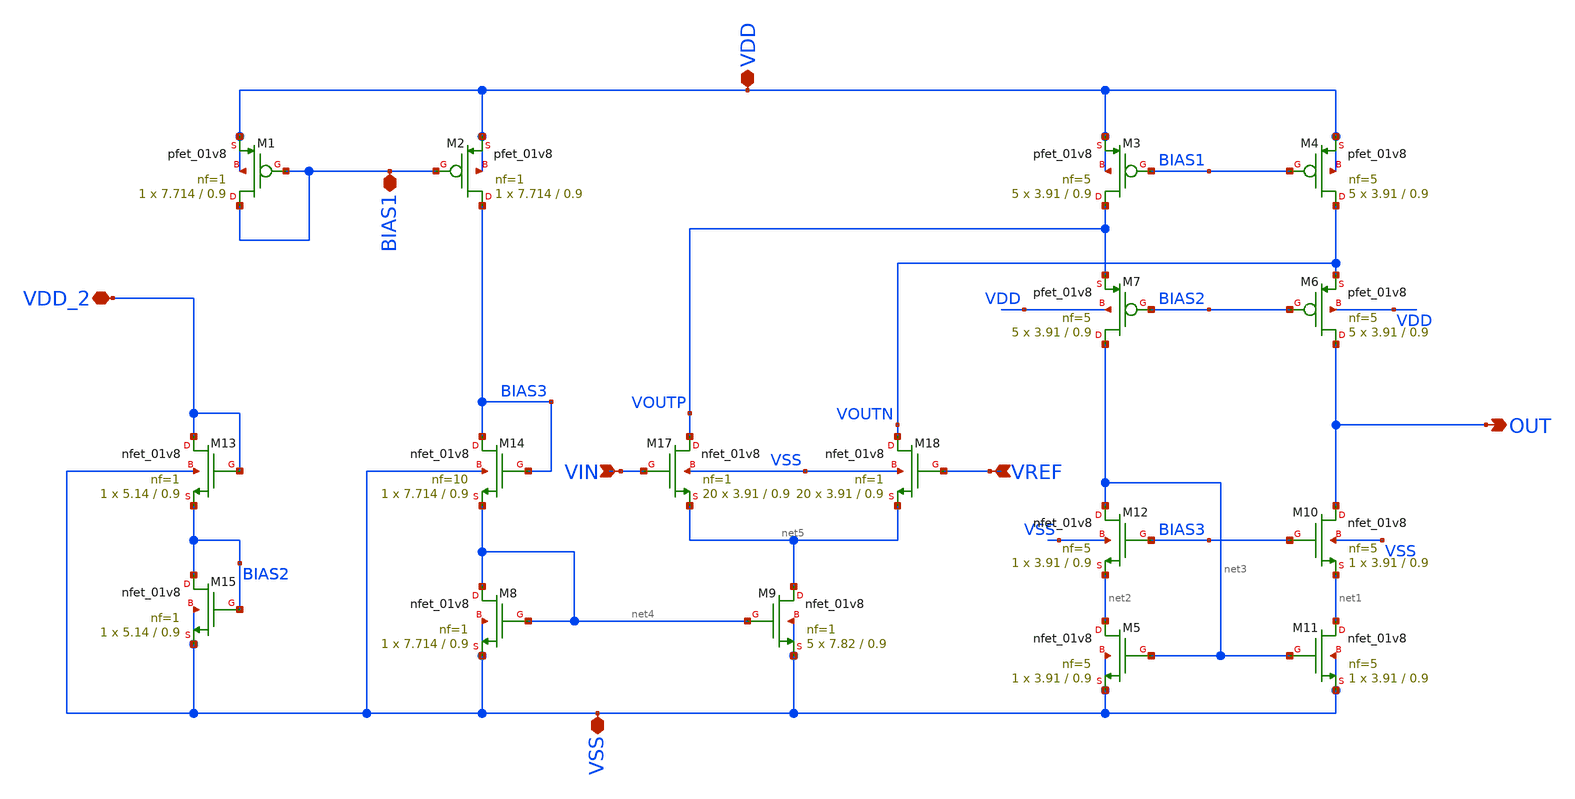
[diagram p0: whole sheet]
** sch_path: xschem/DC_DC_Converter_xschem/OTHERS/DC_DC_Converter_V7/Folded_OPAMP/Folded_OPAMP_previous.sch
**.subckt Folded_OPAMP_previous VSS VDD VDD_2 OUT VIN VREF BIAS1
*.iopin VSS
*.iopin VDD
*.iopin VDD_2
*.opin OUT
*.ipin VIN
*.ipin VREF
*.iopin BIAS1
XM3 VOUTP BIAS1 VDD VDD sky130_fd_pr__pfet_01v8 L=0.9 W=3.91 nf=5 ad='int((nf+1)/2) * W/nf * 0.29' as='int((nf+2)/2) * W/nf * 0.29'
+ pd='2*int((nf+1)/2) * (W/nf + 0.29)' ps='2*int((nf+2)/2) * (W/nf + 0.29)' nrd='0.29 / W' nrs='0.29 / W'
+ sa=0 sb=0 sd=0 mult=5 m=5
XM4 VOUTN BIAS1 VDD VDD sky130_fd_pr__pfet_01v8 L=0.9 W=3.91 nf=5 ad='int((nf+1)/2) * W/nf * 0.29' as='int((nf+2)/2) * W/nf * 0.29'
+ pd='2*int((nf+1)/2) * (W/nf + 0.29)' ps='2*int((nf+2)/2) * (W/nf + 0.29)' nrd='0.29 / W' nrs='0.29 / W'
+ sa=0 sb=0 sd=0 mult=5 m=5
XM6 OUT BIAS2 VOUTN VDD sky130_fd_pr__pfet_01v8 L=0.9 W=3.91 nf=5 ad='int((nf+1)/2) * W/nf * 0.29' as='int((nf+2)/2) * W/nf * 0.29'
+ pd='2*int((nf+1)/2) * (W/nf + 0.29)' ps='2*int((nf+2)/2) * (W/nf + 0.29)' nrd='0.29 / W' nrs='0.29 / W'
+ sa=0 sb=0 sd=0 mult=5 m=5
XM7 net3 BIAS2 VOUTP VDD sky130_fd_pr__pfet_01v8 L=0.9 W=3.91 nf=5 ad='int((nf+1)/2) * W/nf * 0.29' as='int((nf+2)/2) * W/nf * 0.29'
+ pd='2*int((nf+1)/2) * (W/nf + 0.29)' ps='2*int((nf+2)/2) * (W/nf + 0.29)' nrd='0.29 / W' nrs='0.29 / W'
+ sa=0 sb=0 sd=0 mult=5 m=5
XM13 VDD_2 VDD_2 BIAS2 VSS sky130_fd_pr__nfet_01v8 L=0.9 W=5.14 nf=1 ad='int((nf+1)/2) * W/nf * 0.29'
+ as='int((nf+2)/2) * W/nf * 0.29' pd='2*int((nf+1)/2) * (W/nf + 0.29)' ps='2*int((nf+2)/2) * (W/nf + 0.29)'
+ nrd='0.29 / W' nrs='0.29 / W' sa=0 sb=0 sd=0 mult=1 m=1
XM14 BIAS3 BIAS3 net4 VSS sky130_fd_pr__nfet_01v8 L=0.9 W=7.714 nf=10 ad='int((nf+1)/2) * W/nf * 0.29'
+ as='int((nf+2)/2) * W/nf * 0.29' pd='2*int((nf+1)/2) * (W/nf + 0.29)' ps='2*int((nf+2)/2) * (W/nf + 0.29)'
+ nrd='0.29 / W' nrs='0.29 / W' sa=0 sb=0 sd=0 mult=1 m=1
XM15 BIAS2 BIAS2 VSS VSS sky130_fd_pr__nfet_01v8 L=0.9 W=5.14 nf=1 ad='int((nf+1)/2) * W/nf * 0.29' as='int((nf+2)/2) * W/nf * 0.29'
+ pd='2*int((nf+1)/2) * (W/nf + 0.29)' ps='2*int((nf+2)/2) * (W/nf + 0.29)' nrd='0.29 / W' nrs='0.29 / W'
+ sa=0 sb=0 sd=0 mult=1 m=1
XM17 VOUTP VIN net5 VSS sky130_fd_pr__nfet_01v8 L=0.9 W=3.91 nf=1 ad='int((nf+1)/2) * W/nf * 0.29' as='int((nf+2)/2) * W/nf * 0.29'
+ pd='2*int((nf+1)/2) * (W/nf + 0.29)' ps='2*int((nf+2)/2) * (W/nf + 0.29)' nrd='0.29 / W' nrs='0.29 / W'
+ sa=0 sb=0 sd=0 mult=20 m=20
XM18 VOUTN VREF net5 VSS sky130_fd_pr__nfet_01v8 L=0.9 W=3.91 nf=1 ad='int((nf+1)/2) * W/nf * 0.29' as='int((nf+2)/2) * W/nf * 0.29'
+ pd='2*int((nf+1)/2) * (W/nf + 0.29)' ps='2*int((nf+2)/2) * (W/nf + 0.29)' nrd='0.29 / W' nrs='0.29 / W'
+ sa=0 sb=0 sd=0 mult=20 m=20
XM10 OUT BIAS3 net1 VSS sky130_fd_pr__nfet_01v8 L=0.9 W=3.91 nf=5 ad='int((nf+1)/2) * W/nf * 0.29' as='int((nf+2)/2) * W/nf * 0.29'
+ pd='2*int((nf+1)/2) * (W/nf + 0.29)' ps='2*int((nf+2)/2) * (W/nf + 0.29)' nrd='0.29 / W' nrs='0.29 / W'
+ sa=0 sb=0 sd=0 mult=1 m=1
XM12 net3 BIAS3 net2 VSS sky130_fd_pr__nfet_01v8 L=0.9 W=3.91 nf=5 ad='int((nf+1)/2) * W/nf * 0.29' as='int((nf+2)/2) * W/nf * 0.29'
+ pd='2*int((nf+1)/2) * (W/nf + 0.29)' ps='2*int((nf+2)/2) * (W/nf + 0.29)' nrd='0.29 / W' nrs='0.29 / W'
+ sa=0 sb=0 sd=0 mult=1 m=1
XM8 net4 net4 VSS VSS sky130_fd_pr__nfet_01v8 L=0.9 W=7.714 nf=1 ad='int((nf+1)/2) * W/nf * 0.29' as='int((nf+2)/2) * W/nf * 0.29'
+ pd='2*int((nf+1)/2) * (W/nf + 0.29)' ps='2*int((nf+2)/2) * (W/nf + 0.29)' nrd='0.29 / W' nrs='0.29 / W'
+ sa=0 sb=0 sd=0 mult=1 m=1
XM9 net5 net4 VSS VSS sky130_fd_pr__nfet_01v8 L=0.9 W=7.82 nf=1 ad='int((nf+1)/2) * W/nf * 0.29' as='int((nf+2)/2) * W/nf * 0.29'
+ pd='2*int((nf+1)/2) * (W/nf + 0.29)' ps='2*int((nf+2)/2) * (W/nf + 0.29)' nrd='0.29 / W' nrs='0.29 / W'
+ sa=0 sb=0 sd=0 mult=5 m=5
XM5 net2 net3 VSS VSS sky130_fd_pr__nfet_01v8 L=0.9 W=3.91 nf=5 ad='int((nf+1)/2) * W/nf * 0.29' as='int((nf+2)/2) * W/nf * 0.29'
+ pd='2*int((nf+1)/2) * (W/nf + 0.29)' ps='2*int((nf+2)/2) * (W/nf + 0.29)' nrd='0.29 / W' nrs='0.29 / W'
+ sa=0 sb=0 sd=0 mult=1 m=1
XM11 net1 net3 VSS VSS sky130_fd_pr__nfet_01v8 L=0.9 W=3.91 nf=5 ad='int((nf+1)/2) * W/nf * 0.29' as='int((nf+2)/2) * W/nf * 0.29'
+ pd='2*int((nf+1)/2) * (W/nf + 0.29)' ps='2*int((nf+2)/2) * (W/nf + 0.29)' nrd='0.29 / W' nrs='0.29 / W'
+ sa=0 sb=0 sd=0 mult=1 m=1
XM1 BIAS1 BIAS1 VDD VDD sky130_fd_pr__pfet_01v8 L=0.9 W=7.714 nf=1 ad='int((nf+1)/2) * W/nf * 0.29' as='int((nf+2)/2) * W/nf * 0.29'
+ pd='2*int((nf+1)/2) * (W/nf + 0.29)' ps='2*int((nf+2)/2) * (W/nf + 0.29)' nrd='0.29 / W' nrs='0.29 / W'
+ sa=0 sb=0 sd=0 mult=1 m=1
XM2 BIAS3 BIAS1 VDD VDD sky130_fd_pr__pfet_01v8 L=0.9 W=7.714 nf=1 ad='int((nf+1)/2) * W/nf * 0.29' as='int((nf+2)/2) * W/nf * 0.29'
+ pd='2*int((nf+1)/2) * (W/nf + 0.29)' ps='2*int((nf+2)/2) * (W/nf + 0.29)' nrd='0.29 / W' nrs='0.29 / W'
+ sa=0 sb=0 sd=0 mult=1 m=1
**.ends
.end
